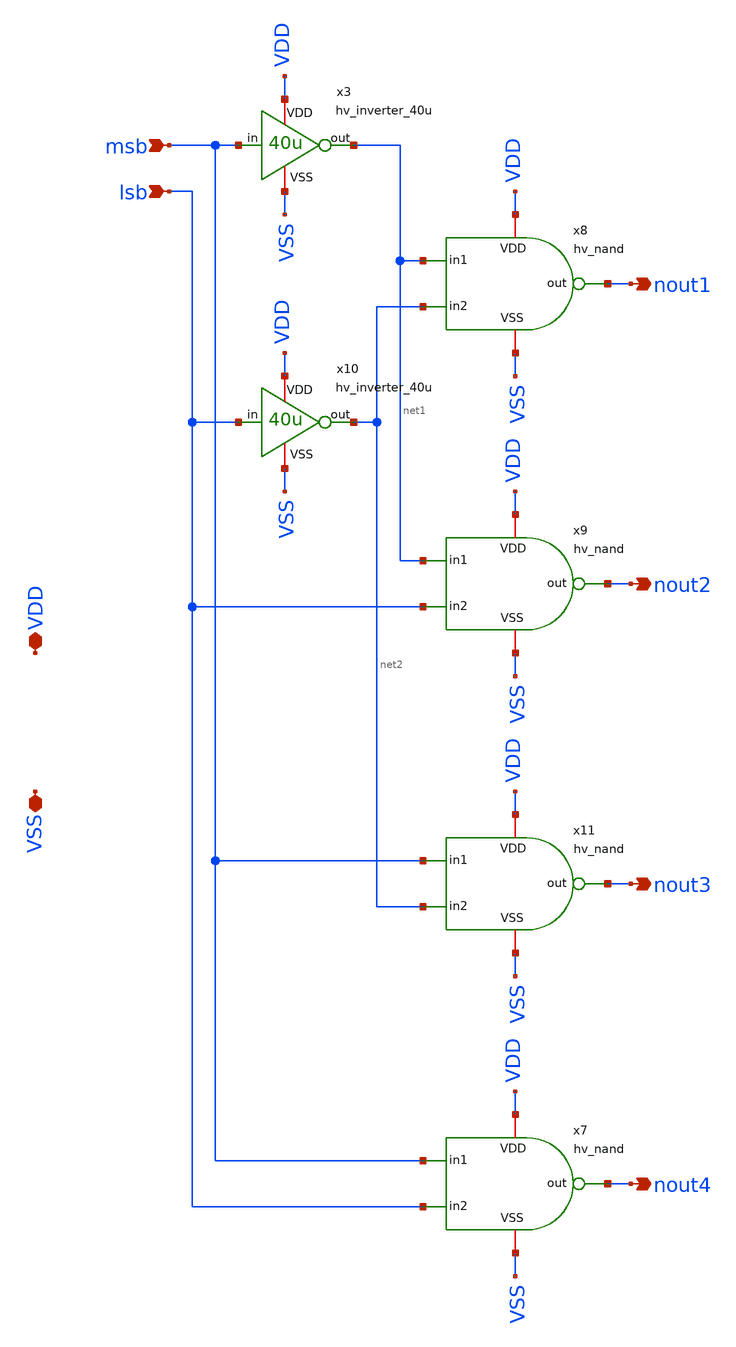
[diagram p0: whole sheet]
** sch_path: macros/heichips26_vcr/macros/switched_capacitor/schematic/xschem/hv_binary_decoder4.sch
**.subckt hv_binary_decoder4 VDD VSS msb lsb nout1 nout2 nout3 nout4
*.iopin VDD
*.iopin VSS
*.ipin msb
*.ipin lsb
*.opin nout1
*.opin nout2
*.opin nout3
*.opin nout4
x3 VDD msb net1 VSS hv_inverter_40u
x7 VDD msb nout4 lsb VSS hv_nand
x9 VDD net1 nout2 lsb VSS hv_nand
x10 VDD lsb net2 VSS hv_inverter_40u
x11 VDD msb nout3 net2 VSS hv_nand
x8 VDD net1 nout1 net2 VSS hv_nand
**.ends

* expanding   symbol:  hv_inverter_40u.sym # of pins=4
** sym_path: macros/heichips26_vcr/macros/switched_capacitor/schematic/xschem/hv_inverter_40u.sym
** sch_path: macros/heichips26_vcr/macros/switched_capacitor/schematic/xschem/hv_inverter_40u.sch
.subckt hv_inverter_40u VDD in out VSS
*.ipin in
*.iopin VDD
*.iopin VSS
*.opin out
XM2 out in VSS VSS sg13_hv_nmos w={n_w} l={n_l} ng={ng} m=1 mm_ok=1
XM3 out in VDD VDD sg13_hv_pmos w={p_w} l={p_l} ng={ng} m=1 mm_ok=1
**** begin user architecture code


.param w   = 10u
.param ng  = 4
.param n_ng = ng
.param n_w = {3u*n_ng}
.param n_l = 0.45u
.param p_ng = ng
.param p_w = {10u*p_ng}
.param p_l = 0.4u


**** end user architecture code
.ends


* expanding   symbol:  hv_nand.sym # of pins=5
** sym_path: macros/heichips26_vcr/macros/switched_capacitor/schematic/xschem/hv_nand.sym
** sch_path: macros/heichips26_vcr/macros/switched_capacitor/schematic/xschem/hv_nand.sch
.subckt hv_nand VDD in1 out in2 VSS
*.ipin in1
*.iopin VDD
*.iopin VSS
*.opin out
*.ipin in2
**** begin user architecture code


.param w   = 10u
.param ng  = 4
.param n_ng = ng
.param n_w = {3u*n_ng}
.param n_l = 0.45u
.param p_ng = ng
.param p_w = {10u*p_ng}
.param p_l = 0.4u


**** end user architecture code
XM2 out in1 net1 VSS sg13_hv_nmos w={n_w} l={n_l} ng={ng} m=1 mm_ok=1
XM3 out in2 VDD VDD sg13_hv_pmos w={p_w} l={p_l} ng={ng} m=1 mm_ok=1
XM1 net1 in2 VSS VSS sg13_hv_nmos w={n_w} l={n_l} ng={ng} m=1 mm_ok=1
XM4 out in1 VDD VDD sg13_hv_pmos w={p_w} l={p_l} ng={ng} m=1 mm_ok=1
.ends

.end
